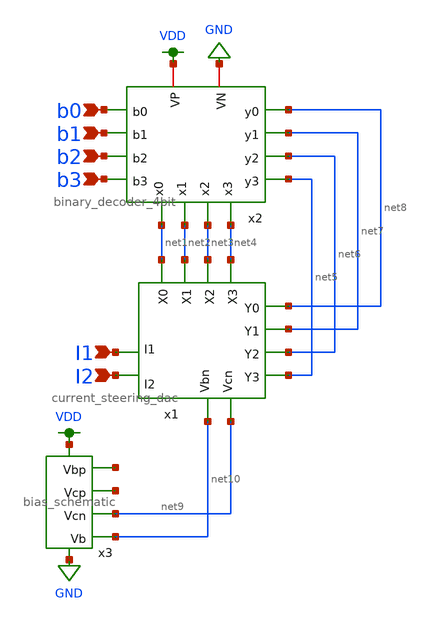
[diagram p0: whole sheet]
** sch_path: lvs/dac_with_decoder.sch
**.subckt dac_with_decoder b0 b1 b2 b3 I1 I2
*.ipin b0
*.ipin b1
*.ipin b2
*.ipin b3
*.ipin I1
*.ipin I2
x2 net8 net1 net2 net7 VDD b0 b1 net3 net6 b2 b3 GND net5 net4 binary_decoder_4bit
x1 net9 net10 net3 net4 I1 I2 net8 net7 net6 net5 net1 net2 current_steering_dac
x3 VDD net11 net12 net9 GND net10 bias_schematic
**.ends
.GLOBAL VDD
.GLOBAL GND
.end
